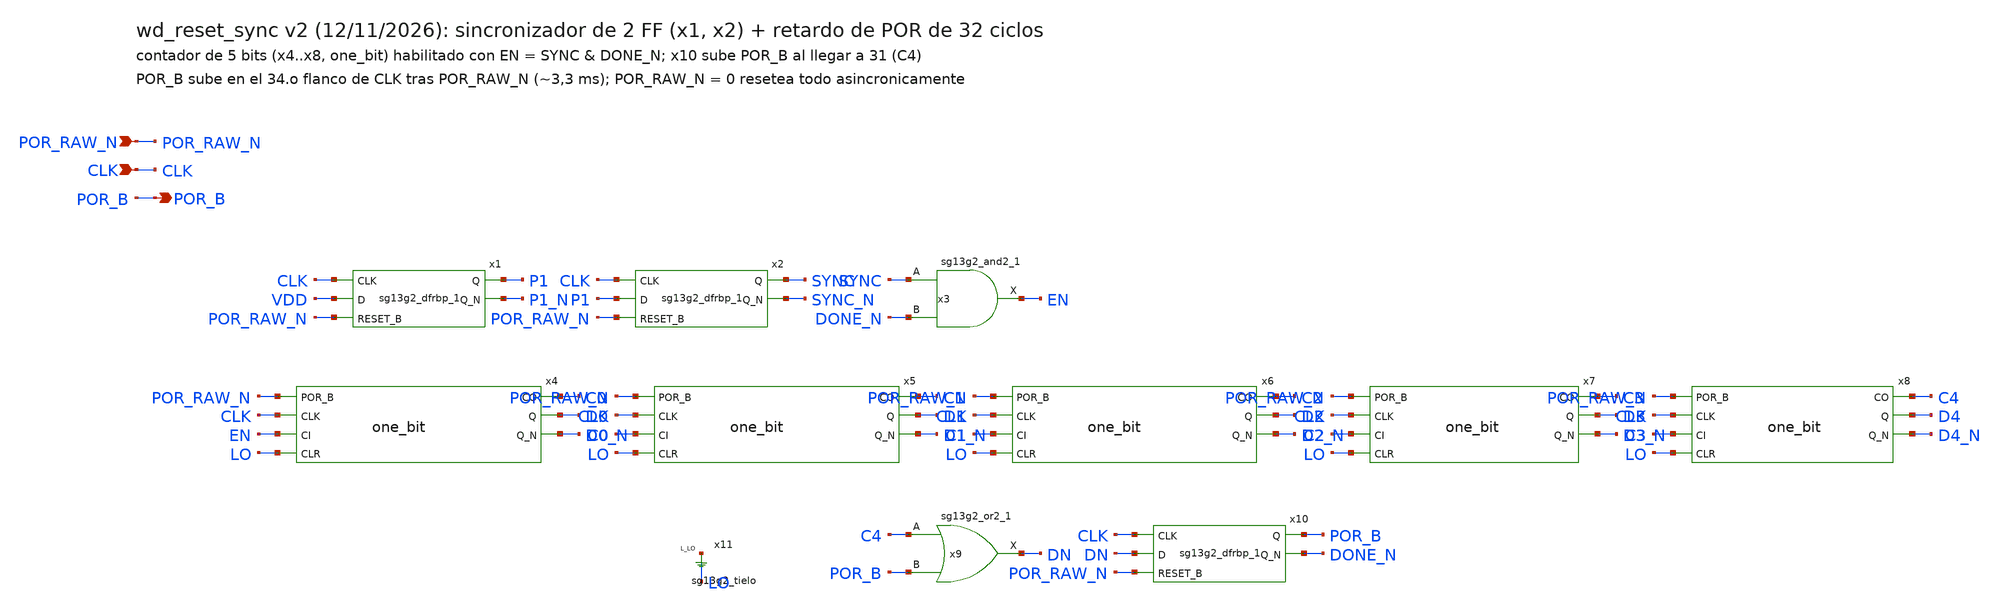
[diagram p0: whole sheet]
** sch_path: design/blocks/por/schematic/wd_reset_sync.sch
**.subckt wd_reset_sync POR_RAW_N CLK POR_B
*.ipin POR_RAW_N
*.ipin CLK
*.opin POR_B
x1 P1 P1_N CLK VDD POR_RAW_N VDD VSS sg13g2_dfrbp_1
x2 SYNC SYNC_N CLK P1 POR_RAW_N VDD VSS sg13g2_dfrbp_1
x3 EN SYNC DONE_N VDD VSS sg13g2_and2_1
x4 C0 POR_RAW_N CLK EN LO D0 D0_N VDD VSS one_bit
x5 C1 POR_RAW_N CLK C0 LO D1 D1_N VDD VSS one_bit
x6 C2 POR_RAW_N CLK C1 LO D2 D2_N VDD VSS one_bit
x7 C3 POR_RAW_N CLK C2 LO D3 D3_N VDD VSS one_bit
x8 C4 POR_RAW_N CLK C3 LO D4 D4_N VDD VSS one_bit
x9 DN C4 POR_B VDD VSS sg13g2_or2_1
x10 POR_B DONE_N CLK DN POR_RAW_N VDD VSS sg13g2_dfrbp_1
x11 LO VDD VSS sg13g2_tielo
**.ends
.end
